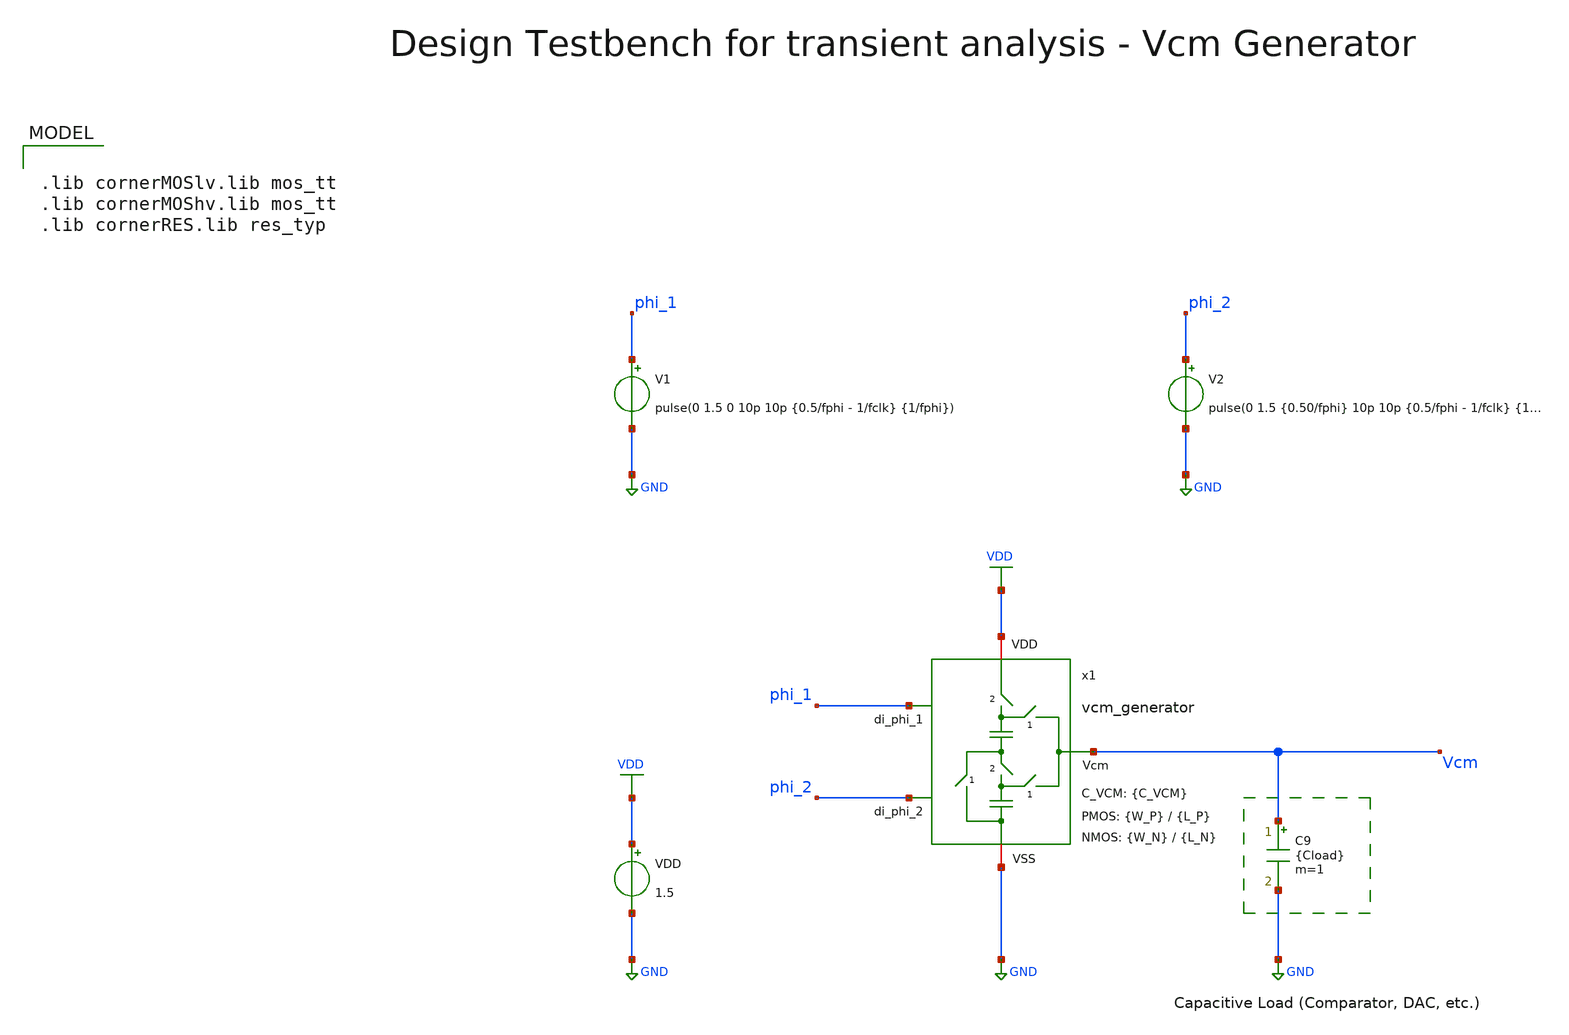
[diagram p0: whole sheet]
** sch_path: SG13G2_ATBS-ADC-main/xschem/vcm_generator/testbenches/vcm_generator_tb_tran.sch
**.subckt vcm_generator_tb_tran
VDD VDD GND 1.5
V1 phi_1 GND pulse(0 1.5 0 10p 10p {0.5/fphi - 1/fclk} {1/fphi})
V2 phi_2 GND pulse(0 1.5 {0.50/fphi} 10p 10p {0.5/fphi - 1/fclk} {1/fphi})
C9 Vcm GND {Cload} m=1
x1 VDD phi_2 phi_1 Vcm GND vcm_generator C_VCM={C_VCM} W_P_VCM={W_P} L_P_VCM={L_P} W_N_VCM={W_N} L_N_VCM={L_N}
**** begin user architecture code

.lib cornerMOSlv.lib mos_tt
.lib cornerMOShv.lib mos_tt
.lib cornerRES.lib res_typ



.param temp=27
.param fclk=8000000
.param fphi=31250
.param Cload=10p
.param C_VCM=1p
.param W_P=1.0u
.param L_P=0.13u
.param W_N=1.0u
.param L_N=0.13u
.ic v(Vcm)=0
.options savecurrents reltol=1e-3 abstol=1e-12 gmin=1e-12
.control

* save all
save phi_1 x1.di_phi_1_n phi_2 x1.di_phi_2_n Vcm

* User Constants
let tstep = 500n
let tstart = 0.5m
let tstop = 1m

* Operating Point Analysis
op
remzerovec
write vcm_generator_tb_tran.raw
set appendwrite

* Transient Analysis
tran $&tstep $&tstop
write vcm_generator_tb_tran.raw

plot v(phi_1) v(x1.di_phi_1_n) v(phi_2) v(x1.di_phi_2_n)
plot v(Vcm) v(phi_1) v(phi_2)

* Measurements
meas tran Vcm_at_tstop FIND v(Vcm) at=tstop

* tsettle at 99% Vcm
meas tran tsettle WHEN v(Vcm)=0.7425 RISE=1

* Writing Data
set wr_singlescale
set wr_vecnames
let di_phi_1_n = x1.di_phi_1_n
let di_phi_2_n = x1.di_phi_2_n
wrdata /foss/designs/SG13G2_ATBS-ADC-main/python/plot_simulations/data/vcm_generator_tb_tran.txt
+ v(phi_1) v(di_phi_1_n) v(phi_2) v(di_phi_2_n) v(Vcm)

*quit
.endc

**** end user architecture code
**.ends

* expanding   symbol:  vcm_generator/vcm_generator.sym # of pins=5
** sym_path: SG13G2_ATBS-ADC-main/xschem/vcm_generator/vcm_generator.sym
** sch_path: SG13G2_ATBS-ADC-main/xschem/vcm_generator/vcm_generator.sch
.subckt vcm_generator VDD di_phi_2 di_phi_1 Vcm VSS  C_VCM=1p W_P_VCM=1.0u L_P_VCM=0.13u
+ W_N_VCM=1.0u L_N_VCM=0.13u
*.iopin VDD
*.opin Vcm
*.iopin VSS
*.ipin di_phi_1
*.ipin di_phi_2
x1 VDD di_phi_2 VSS net1 VDD di_phi_2_n transmission_gate_lv_wo_dummy W_P=W_P_VCM L_P=L_P_VCM
+ W_N=W_N_VCM L_N=L_N_VCM
x2 VDD di_phi_1 VSS Vcm net1 di_phi_1_n transmission_gate_lv_wo_dummy W_P=W_P_VCM L_P=L_P_VCM
+ W_N=W_N_VCM L_N=L_N_VCM
x3 VDD di_phi_2 VSS net3 net2 di_phi_2_n transmission_gate_lv_wo_dummy W_P=W_P_VCM L_P=L_P_VCM
+ W_N=W_N_VCM L_N=L_N_VCM
x4 VDD di_phi_1 VSS Vcm net3 di_phi_1_n transmission_gate_lv_wo_dummy W_P=W_P_VCM L_P=L_P_VCM
+ W_N=W_N_VCM L_N=L_N_VCM
x5 VDD di_phi_1 VSS VSS net2 di_phi_1_n transmission_gate_lv_wo_dummy W_P=W_P_VCM L_P=L_P_VCM
+ W_N=W_N_VCM L_N=L_N_VCM
x9 VDD di_phi_1 di_phi_1_n VSS inverter_lv W_P=W_P_VCM L_P=L_P_VCM W_N=W_N_VCM L_N=L_N_VCM
x8 VDD di_phi_2 di_phi_2_n VSS inverter_lv W_P=W_P_VCM L_P=L_P_VCM W_N=W_N_VCM L_N=L_N_VCM
C1 net1 net2 C_VCM m=1
C2 net3 VSS C_VCM m=1
.ends


* expanding   symbol:  transmission_gate/transmission_gate_lv_wo_dummy.sym # of pins=6
** sym_path: SG13G2_ATBS-ADC-main/xschem/transmission_gate/transmission_gate_lv_wo_dummy.sym
** sch_path: SG13G2_ATBS-ADC-main/xschem/transmission_gate/transmission_gate_lv_wo_dummy.sch
.subckt transmission_gate_lv_wo_dummy VDD di_tg_ctrl VSS v_b v_a di_tg_ctrl_n  W_P=1.0u L_P=0.13u
+ W_N=1.0u L_N=0.13u
*.iopin v_a
*.iopin v_b
*.iopin VDD
*.iopin VSS
*.ipin di_tg_ctrl
*.ipin di_tg_ctrl_n
XM1 v_a di_tg_ctrl v_b VSS sg13_lv_nmos w=W_N l=L_N ng=1 m=1 mm_ok=1
XM2 v_a di_tg_ctrl_n v_b VDD sg13_lv_pmos w=W_P l=L_P ng=1 m=1 mm_ok=1
.ends


* expanding   symbol:  inverter/inverter_lv.sym # of pins=4
** sym_path: SG13G2_ATBS-ADC-main/xschem/inverter/inverter_lv.sym
** sch_path: SG13G2_ATBS-ADC-main/xschem/inverter/inverter_lv.sch
.subckt inverter_lv VDD vin vout VSS  W_P=3.0u L_P=0.13u W_N=1.0u L_N=0.13u
*.ipin vin
*.iopin VDD
*.iopin VSS
*.opin vout
XM1 vout vin VDD VDD sg13_lv_pmos w=W_P l=L_P ng=1 m=1 mm_ok=1
XM2 vout vin VSS VSS sg13_lv_nmos w=W_N l=L_N ng=1 m=1 mm_ok=1
.ends

.GLOBAL GND
.GLOBAL VDD
.end
